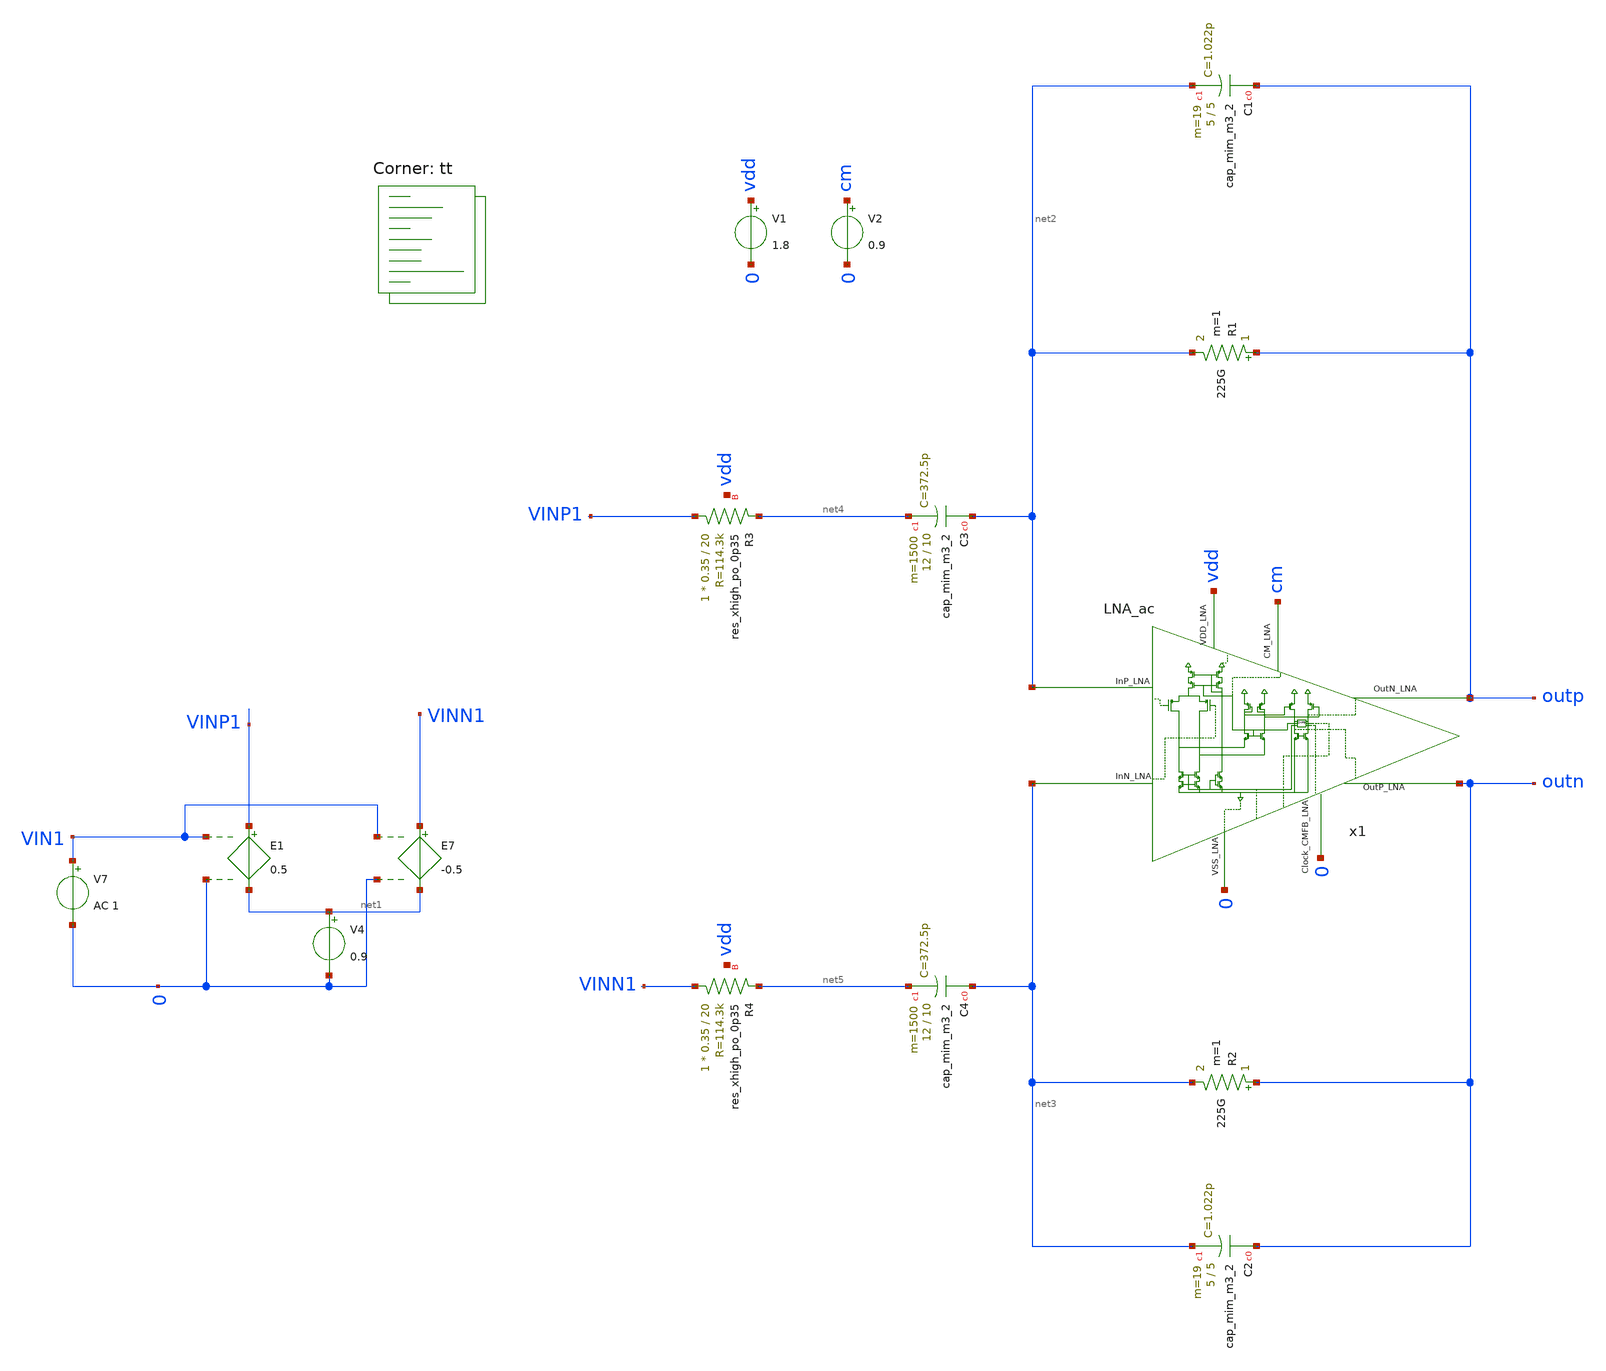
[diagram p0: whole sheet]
** sch_path: CL_ac.sch
**.subckt CL_ac
x1 net3 net2 vdd cm outp outn 0 0 LNA_ac
V1 vdd 0 1.8
V2 cm 0 0.9
E1 VINP1 net1 VIN1 0 0.5
E7 VINN1 net1 VIN1 0 -0.5
V4 net1 0 0.9
V7 VIN1 0 AC 1
R1 outp net2 225G m=1
XC1 outp net2 sky130_fd_pr__cap_mim_m3_2 W=5 L=5 MF=19 m=19
XC2 outn net3 sky130_fd_pr__cap_mim_m3_2 W=5 L=5 MF=19 m=19
R2 outn net3 225G m=1
XC3 net2 net4 sky130_fd_pr__cap_mim_m3_2 W=12 L=10 MF=1500 m=1500
XC4 net3 net5 sky130_fd_pr__cap_mim_m3_2 W=12 L=10 MF=1500 m=1500
XR3 VINP1 net4 vdd sky130_fd_pr__res_xhigh_po_0p35 L=20 mult=1 m=1
XR4 VINN1 net5 vdd sky130_fd_pr__res_xhigh_po_0p35 L=20 mult=1 m=1
**** begin user architecture code
.lib $::SKYWATER_MODELS/sky130.lib.spice tt


.options savecurrents
*ic v(VM5)=0.9 v(VM6)=0.9
.control


save all

save @m.xm11.msky130_fd_pr__pfet_01v8_lvt[id]
save @m.xm11.msky130_fd_pr__pfet_01v8_lvt[vgs]


*nmos
save @m.xm3.msky130_fd_pr__nfet_01v8_lvt[vgs]
save @m.xm3.msky130_fd_pr__nfet_01v8_lvt[vth]
save @m.xm3.msky130_fd_pr__nfet_01v8_lvt[vds]

save @m.xm6.msky130_fd_pr__nfet_01v8_lvt[vgs]
save @m.xm6.msky130_fd_pr__nfet_01v8_lvt[vth]
save @m.xm6.msky130_fd_pr__nfet_01v8_lvt[vds]

save @m.xm8.msky130_fd_pr__nfet_01v8_lvt[vgs]
save @m.xm8.msky130_fd_pr__nfet_01v8_lvt[vth]
save @m.xm8.msky130_fd_pr__nfet_01v8_lvt[vds]

save @m.xm9.msky130_fd_pr__nfet_01v8_lvt[vgs]
save @m.xm9.msky130_fd_pr__nfet_01v8_lvt[vth]
save @m.xm9.msky130_fd_pr__nfet_01v8_lvt[vds]

save @m.xm18.msky130_fd_pr__nfet_01v8_lvt[vgs]
save @m.xm18.msky130_fd_pr__nfet_01v8_lvt[vth]
save @m.xm18.msky130_fd_pr__nfet_01v8_lvt[vds]

save @m.xm19.msky130_fd_pr__nfet_01v8_lvt[vgs]
save @m.xm19.msky130_fd_pr__nfet_01v8_lvt[vth]
save @m.xm19.msky130_fd_pr__nfet_01v8_lvt[vds]

save @m.xm25.msky130_fd_pr__nfet_01v8_lvt[vgs]
save @m.xm25.msky130_fd_pr__nfet_01v8_lvt[vth]
save @m.xm25.msky130_fd_pr__nfet_01v8_lvt[vds]

*pmos

save @m.xm1.msky130_fd_pr__pfet_01v8_lvt[vgs]
save @m.xm1.msky130_fd_pr__pfet_01v8_lvt[vth]
save @m.xm1.msky130_fd_pr__pfet_01v8_lvt[vds]


save @m.xm2.msky130_fd_pr__pfet_01v8_lvt[vgs]
save @m.xm2.msky130_fd_pr__pfet_01v8_lvt[vth]
save @m.xm2.msky130_fd_pr__pfet_01v8_lvt[vds]


save @m.xm10.msky130_fd_pr__pfet_01v8_lvt[vgs]
save @m.xm10.msky130_fd_pr__pfet_01v8_lvt[vth]
save @m.xm10.msky130_fd_pr__pfet_01v8_lvt[vds]

save @m.xm13.msky130_fd_pr__pfet_01v8_lvt[vgs]
save @m.xm13.msky130_fd_pr__pfet_01v8_lvt[vth]
save @m.xm13.msky130_fd_pr__pfet_01v8_lvt[vds]

save @m.xm4.msky130_fd_pr__pfet_01v8_lvt[vgs]
save @m.xm4.msky130_fd_pr__pfet_01v8_lvt[vth]
save @m.xm4.msky130_fd_pr__pfet_01v8_lvt[vds]

save @m.xm5.msky130_fd_pr__pfet_01v8_lvt[vgs]
save @m.xm5.msky130_fd_pr__pfet_01v8_lvt[vth]
save @m.xm5.msky130_fd_pr__pfet_01v8_lvt[vds]

save @m.xm16.msky130_fd_pr__pfet_01v8_lvt[vgs]
save @m.xm16.msky130_fd_pr__pfet_01v8_lvt[vth]
save @m.xm16.msky130_fd_pr__pfet_01v8_lvt[vds]

save @m.xm17.msky130_fd_pr__pfet_01v8_lvt[vgs]
save @m.xm17.msky130_fd_pr__pfet_01v8_lvt[vth]
save @m.xm17.msky130_fd_pr__pfet_01v8_lvt[vds]

save @m.xm3.msky130_fd_pr__pfet_01v8_lvt[vgs]
save @m.xm3.msky130_fd_pr__pfet_01v8_lvt[vth]
save @m.xm3.msky130_fd_pr__pfet_01v8_lvt[vds]

save @m.xm20.msky130_fd_pr__pfet_01v8_lvt[vgs]
save @m.xm20.msky130_fd_pr__pfet_01v8_lvt[vth]
save @m.xm20.msky130_fd_pr__pfet_01v8_lvt[vds]

save @m.xm2.msky130_fd_pr__pfet_01v8_lvt[vgs]
save @m.xm2.msky130_fd_pr__pfet_01v8_lvt[vth]
save @m.xm2.msky130_fd_pr__pfet_01v8_lvt[vds]

save @m.xm21.msky130_fd_pr__pfet_01v8_lvt[vgs]
save @m.xm21.msky130_fd_pr__pfet_01v8_lvt[vth]
save @m.xm21.msky130_fd_pr__pfet_01v8_lvt[vds]

save @m.xm7.msky130_fd_pr__nfet_01v8_lvt[vth]

save @m.xm1.msky130_fd_pr__pfet_01v8[vgs]

save @m.xm1.msky130_fd_pr__nfet_01v8_lvt[gm]


save @m.xm1.msky130_fd_pr__nfet_01v8_lvt[gds]
save @m.xm2.msky130_fd_pr__pfet_01v8_lvt[gm]

save @m.xm23.msky130_fd_pr__nfet_01v8[cgs]
save @m.xm4.msky130_fd_pr__pfet_01v8[cgs]
save @m.xm2.msky130_fd_pr__pfet_01v8_lvt[cgs]



save @m.xm2.msky130_fd_pr__pfet_01v8_lvt[gds]


op
write testbench.raw
*set appendwrite


.endc
.control



*tran 50u 1500m
*save all
*plot v(Outp)-v(outn)


noise V(Outp,Outn) V7 dec 100 0.1 128
print inoise_total onoise_total
setplot noise1
plot inoise_spectrum

ac dec 10 0.1 20k
let gaind=(v(outp)-v(outn))/(v(VINP1)-v(VINN1))
plot db(gaind)


.endc






.include $::SKYWATER_STDCELLS/sky130_fd_sc_hd.spice

**** end user architecture code
**.ends
.end
